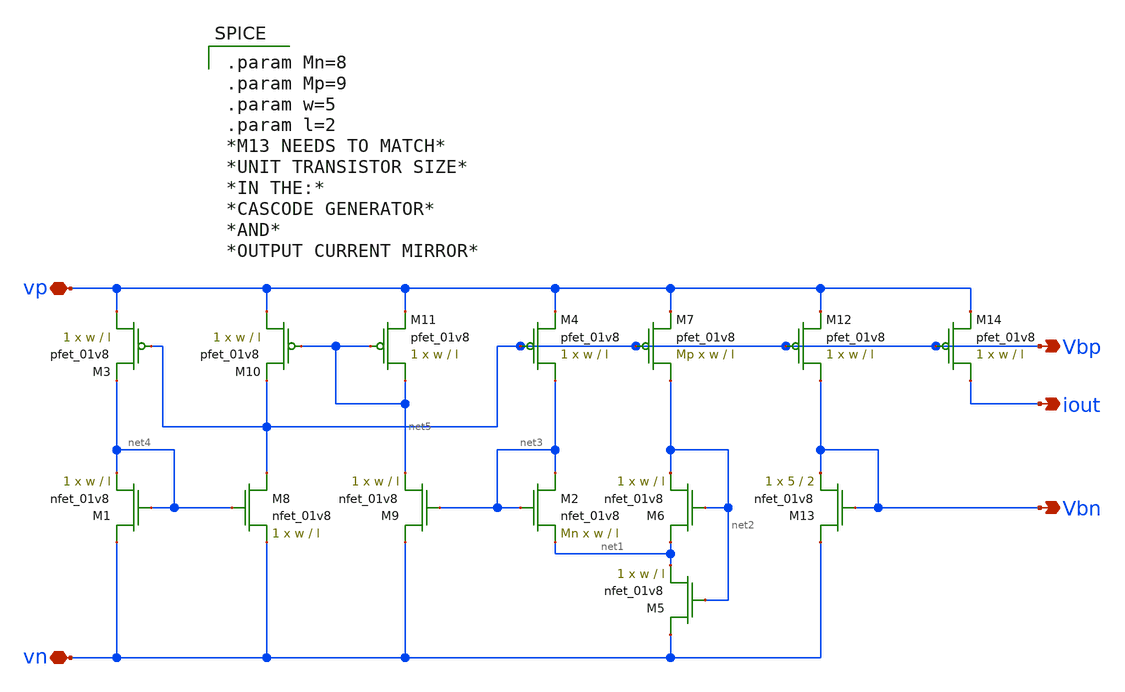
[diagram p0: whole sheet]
** sch_path: schematic/bias_current.sch
**.subckt bias_current vp vn iout Vbp Vbn
*.iopin vp
*.iopin vn
*.opin iout
*.opin Vbp
*.opin Vbn
XM1 vn net4 net4 GND sky130_fd_pr__nfet_01v8 L=l W=w nf=1 ad='int((nf+1)/2) * W/nf * 0.29' as='int((nf+2)/2) * W/nf * 0.29'
+ pd='2*int((nf+1)/2) * (W/nf + 0.29)' ps='2*int((nf+2)/2) * (W/nf + 0.29)' nrd='0.29 / W' nrs='0.29 / W'
+ sa=0 sb=0 sd=0 mult=1 m=1
XM2 net3 net3 net1 GND sky130_fd_pr__nfet_01v8 L=l W=w nf=1 ad='int((nf+1)/2) * W/nf * 0.29' as='int((nf+2)/2) * W/nf * 0.29'
+ pd='2*int((nf+1)/2) * (W/nf + 0.29)' ps='2*int((nf+2)/2) * (W/nf + 0.29)' nrd='0.29 / W' nrs='0.29 / W'
+ sa=0 sb=0 sd=0 mult=Mn m=Mn
XM3 vp Vbp net4 VDD sky130_fd_pr__pfet_01v8 L=l W=w nf=1 ad='int((nf+1)/2) * W/nf * 0.29' as='int((nf+2)/2) * W/nf * 0.29'
+ pd='2*int((nf+1)/2) * (W/nf + 0.29)' ps='2*int((nf+2)/2) * (W/nf + 0.29)' nrd='0.29 / W' nrs='0.29 / W'
+ sa=0 sb=0 sd=0 mult=1 m=1
XM4 net3 Vbp vp VDD sky130_fd_pr__pfet_01v8 L=l W=w nf=1 ad='int((nf+1)/2) * W/nf * 0.29' as='int((nf+2)/2) * W/nf * 0.29'
+ pd='2*int((nf+1)/2) * (W/nf + 0.29)' ps='2*int((nf+2)/2) * (W/nf + 0.29)' nrd='0.29 / W' nrs='0.29 / W'
+ sa=0 sb=0 sd=0 mult=1 m=1
XM5 vn net2 net1 GND sky130_fd_pr__nfet_01v8 L=l W=w nf=1 ad='int((nf+1)/2) * W/nf * 0.29' as='int((nf+2)/2) * W/nf * 0.29'
+ pd='2*int((nf+1)/2) * (W/nf + 0.29)' ps='2*int((nf+2)/2) * (W/nf + 0.29)' nrd='0.29 / W' nrs='0.29 / W'
+ sa=0 sb=0 sd=0 mult=1 m=1
XM6 net1 net2 net2 GND sky130_fd_pr__nfet_01v8 L=l W=w nf=1 ad='int((nf+1)/2) * W/nf * 0.29' as='int((nf+2)/2) * W/nf * 0.29'
+ pd='2*int((nf+1)/2) * (W/nf + 0.29)' ps='2*int((nf+2)/2) * (W/nf + 0.29)' nrd='0.29 / W' nrs='0.29 / W'
+ sa=0 sb=0 sd=0 mult=1 m=1
XM7 net2 Vbp vp VDD sky130_fd_pr__pfet_01v8 L=l W=w nf=1 ad='int((nf+1)/2) * W/nf * 0.29' as='int((nf+2)/2) * W/nf * 0.29'
+ pd='2*int((nf+1)/2) * (W/nf + 0.29)' ps='2*int((nf+2)/2) * (W/nf + 0.29)' nrd='0.29 / W' nrs='0.29 / W'
+ sa=0 sb=0 sd=0 mult=Mp m=Mp
XM8 Vbp net4 vn GND sky130_fd_pr__nfet_01v8 L=l W=w nf=1 ad='int((nf+1)/2) * W/nf * 0.29' as='int((nf+2)/2) * W/nf * 0.29'
+ pd='2*int((nf+1)/2) * (W/nf + 0.29)' ps='2*int((nf+2)/2) * (W/nf + 0.29)' nrd='0.29 / W' nrs='0.29 / W'
+ sa=0 sb=0 sd=0 mult=1 m=1
XM9 vn net3 net5 GND sky130_fd_pr__nfet_01v8 L=l W=w nf=1 ad='int((nf+1)/2) * W/nf * 0.29' as='int((nf+2)/2) * W/nf * 0.29'
+ pd='2*int((nf+1)/2) * (W/nf + 0.29)' ps='2*int((nf+2)/2) * (W/nf + 0.29)' nrd='0.29 / W' nrs='0.29 / W'
+ sa=0 sb=0 sd=0 mult=1 m=1
XM10 vp net5 Vbp VDD sky130_fd_pr__pfet_01v8 L=l W=w nf=1 ad='int((nf+1)/2) * W/nf * 0.29' as='int((nf+2)/2) * W/nf * 0.29'
+ pd='2*int((nf+1)/2) * (W/nf + 0.29)' ps='2*int((nf+2)/2) * (W/nf + 0.29)' nrd='0.29 / W' nrs='0.29 / W'
+ sa=0 sb=0 sd=0 mult=1 m=1
XM11 net5 net5 vp VDD sky130_fd_pr__pfet_01v8 L=l W=w nf=1 ad='int((nf+1)/2) * W/nf * 0.29' as='int((nf+2)/2) * W/nf * 0.29'
+ pd='2*int((nf+1)/2) * (W/nf + 0.29)' ps='2*int((nf+2)/2) * (W/nf + 0.29)' nrd='0.29 / W' nrs='0.29 / W'
+ sa=0 sb=0 sd=0 mult=1 m=1
XM12 Vbn Vbp vp VDD sky130_fd_pr__pfet_01v8 L=l W=w nf=1 ad='int((nf+1)/2) * W/nf * 0.29' as='int((nf+2)/2) * W/nf * 0.29'
+ pd='2*int((nf+1)/2) * (W/nf + 0.29)' ps='2*int((nf+2)/2) * (W/nf + 0.29)' nrd='0.29 / W' nrs='0.29 / W'
+ sa=0 sb=0 sd=0 mult=1 m=1
XM13 vn Vbn Vbn GND sky130_fd_pr__nfet_01v8 L=2 W=5 nf=1 ad='int((nf+1)/2) * W/nf * 0.29' as='int((nf+2)/2) * W/nf * 0.29'
+ pd='2*int((nf+1)/2) * (W/nf + 0.29)' ps='2*int((nf+2)/2) * (W/nf + 0.29)' nrd='0.29 / W' nrs='0.29 / W'
+ sa=0 sb=0 sd=0 mult=1 m=1
XM14 iout Vbp vp VDD sky130_fd_pr__pfet_01v8 L=l W=w nf=1 ad='int((nf+1)/2) * W/nf * 0.29' as='int((nf+2)/2) * W/nf * 0.29'
+ pd='2*int((nf+1)/2) * (W/nf + 0.29)' ps='2*int((nf+2)/2) * (W/nf + 0.29)' nrd='0.29 / W' nrs='0.29 / W'
+ sa=0 sb=0 sd=0 mult=1 m=1
**** begin user architecture code

.param Mn=8
.param Mp=9
.param w=5
.param l=2
*M13 NEEDS TO MATCH*
*UNIT TRANSISTOR SIZE*
*IN THE:*
*CASCODE GENERATOR*
*AND*
*OUTPUT CURRENT MIRROR*

**** end user architecture code
**.ends
.end
